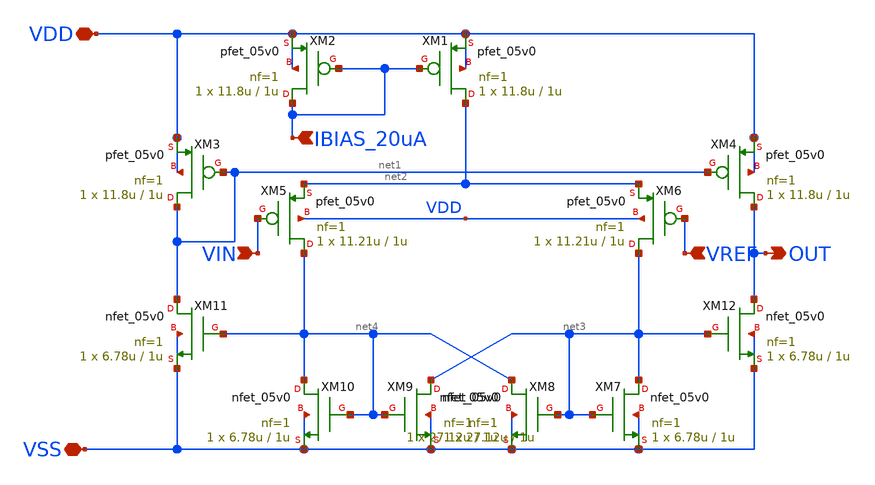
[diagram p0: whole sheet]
** sch_path: designs/hyst-comparator/comp_hyst.sch
**.subckt comp_hyst VIN VREF OUT IBIAS_20uA VDD VSS
*.ipin VIN
*.ipin VREF
*.opin OUT
*.ipin IBIAS_20uA
*.iopin VDD
*.iopin VSS
XM1 net2 IBIAS_20uA VDD VDD pfet_05v0 L=1u W=11.8u nf=1 ad='int((nf+1)/2) * W/nf * 0.18u' as='int((nf+2)/2) * W/nf * 0.18u'
+ pd='2*int((nf+1)/2) * (W/nf + 0.18u)' ps='2*int((nf+2)/2) * (W/nf + 0.18u)' nrd='0.18u / W' nrs='0.18u / W'
+ sa=0 sb=0 sd=0 m=1
XM2 IBIAS_20uA IBIAS_20uA VDD VDD pfet_05v0 L=1u W=11.8u nf=1 ad='int((nf+1)/2) * W/nf * 0.18u' as='int((nf+2)/2) * W/nf * 0.18u'
+ pd='2*int((nf+1)/2) * (W/nf + 0.18u)' ps='2*int((nf+2)/2) * (W/nf + 0.18u)' nrd='0.18u / W' nrs='0.18u / W'
+ sa=0 sb=0 sd=0 m=1
XM3 net1 net1 VDD VDD pfet_05v0 L=1u W=11.8u nf=1 ad='int((nf+1)/2) * W/nf * 0.18u' as='int((nf+2)/2) * W/nf * 0.18u'
+ pd='2*int((nf+1)/2) * (W/nf + 0.18u)' ps='2*int((nf+2)/2) * (W/nf + 0.18u)' nrd='0.18u / W' nrs='0.18u / W'
+ sa=0 sb=0 sd=0 m=1
XM4 OUT net1 VDD VDD pfet_05v0 L=1u W=11.8u nf=1 ad='int((nf+1)/2) * W/nf * 0.18u' as='int((nf+2)/2) * W/nf * 0.18u'
+ pd='2*int((nf+1)/2) * (W/nf + 0.18u)' ps='2*int((nf+2)/2) * (W/nf + 0.18u)' nrd='0.18u / W' nrs='0.18u / W'
+ sa=0 sb=0 sd=0 m=1
XM5 net4 VIN net2 VDD pfet_05v0 L=1u W=11.21u nf=1 ad='int((nf+1)/2) * W/nf * 0.18u' as='int((nf+2)/2) * W/nf * 0.18u'
+ pd='2*int((nf+1)/2) * (W/nf + 0.18u)' ps='2*int((nf+2)/2) * (W/nf + 0.18u)' nrd='0.18u / W' nrs='0.18u / W'
+ sa=0 sb=0 sd=0 m=1
XM6 net3 VREF net2 VDD pfet_05v0 L=1u W=11.21u nf=1 ad='int((nf+1)/2) * W/nf * 0.18u' as='int((nf+2)/2) * W/nf * 0.18u'
+ pd='2*int((nf+1)/2) * (W/nf + 0.18u)' ps='2*int((nf+2)/2) * (W/nf + 0.18u)' nrd='0.18u / W' nrs='0.18u / W'
+ sa=0 sb=0 sd=0 m=1
XM7 net3 net3 VSS VSS nfet_05v0 L=1u W=6.78u nf=1 ad='int((nf+1)/2) * W/nf * 0.18u' as='int((nf+2)/2) * W/nf * 0.18u'
+ pd='2*int((nf+1)/2) * (W/nf + 0.18u)' ps='2*int((nf+2)/2) * (W/nf + 0.18u)' nrd='0.18u / W' nrs='0.18u / W'
+ sa=0 sb=0 sd=0 m=1
XM8 net4 net3 VSS VSS nfet_05v0 L=1u W=27.12u nf=1 ad='int((nf+1)/2) * W/nf * 0.18u' as='int((nf+2)/2) * W/nf * 0.18u'
+ pd='2*int((nf+1)/2) * (W/nf + 0.18u)' ps='2*int((nf+2)/2) * (W/nf + 0.18u)' nrd='0.18u / W' nrs='0.18u / W'
+ sa=0 sb=0 sd=0 m=1
XM9 net3 net4 VSS VSS nfet_05v0 L=1u W=27.12u nf=1 ad='int((nf+1)/2) * W/nf * 0.18u' as='int((nf+2)/2) * W/nf * 0.18u'
+ pd='2*int((nf+1)/2) * (W/nf + 0.18u)' ps='2*int((nf+2)/2) * (W/nf + 0.18u)' nrd='0.18u / W' nrs='0.18u / W'
+ sa=0 sb=0 sd=0 m=1
XM10 net4 net4 VSS VSS nfet_05v0 L=1u W=6.78u nf=1 ad='int((nf+1)/2) * W/nf * 0.18u' as='int((nf+2)/2) * W/nf * 0.18u'
+ pd='2*int((nf+1)/2) * (W/nf + 0.18u)' ps='2*int((nf+2)/2) * (W/nf + 0.18u)' nrd='0.18u / W' nrs='0.18u / W'
+ sa=0 sb=0 sd=0 m=1
XM11 net1 net4 VSS VSS nfet_05v0 L=1u W=6.78u nf=1 ad='int((nf+1)/2) * W/nf * 0.18u' as='int((nf+2)/2) * W/nf * 0.18u'
+ pd='2*int((nf+1)/2) * (W/nf + 0.18u)' ps='2*int((nf+2)/2) * (W/nf + 0.18u)' nrd='0.18u / W' nrs='0.18u / W'
+ sa=0 sb=0 sd=0 m=1
XM12 OUT net3 VSS VSS nfet_05v0 L=1u W=6.78u nf=1 ad='int((nf+1)/2) * W/nf * 0.18u' as='int((nf+2)/2) * W/nf * 0.18u'
+ pd='2*int((nf+1)/2) * (W/nf + 0.18u)' ps='2*int((nf+2)/2) * (W/nf + 0.18u)' nrd='0.18u / W' nrs='0.18u / W'
+ sa=0 sb=0 sd=0 m=1
**.ends
.end
